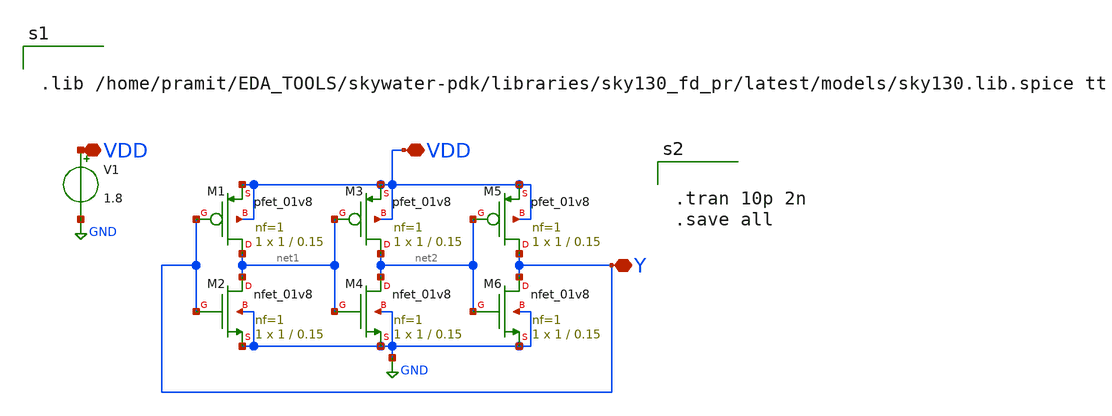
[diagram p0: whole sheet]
** sch_path: week4/schematic/ring_osc.sch
**.subckt ring_osc VDD Y VDD
*.iopin VDD
*.iopin Y
*.iopin VDD
XM1 net1 Y VDD VDD sky130_fd_pr__pfet_01v8 L=0.15 W=1 nf=1 ad='int((nf+1)/2) * W/nf * 0.29' as='int((nf+2)/2) * W/nf * 0.29'
+ pd='2*int((nf+1)/2) * (W/nf + 0.29)' ps='2*int((nf+2)/2) * (W/nf + 0.29)' nrd='0.29 / W' nrs='0.29 / W'
+ sa=0 sb=0 sd=0 mult=1 m=1
XM2 net1 Y GND GND sky130_fd_pr__nfet_01v8 L=0.15 W=1 nf=1 ad='int((nf+1)/2) * W/nf * 0.29' as='int((nf+2)/2) * W/nf * 0.29'
+ pd='2*int((nf+1)/2) * (W/nf + 0.29)' ps='2*int((nf+2)/2) * (W/nf + 0.29)' nrd='0.29 / W' nrs='0.29 / W'
+ sa=0 sb=0 sd=0 mult=1 m=1
XM3 net2 net1 VDD VDD sky130_fd_pr__pfet_01v8 L=0.15 W=1 nf=1 ad='int((nf+1)/2) * W/nf * 0.29' as='int((nf+2)/2) * W/nf * 0.29'
+ pd='2*int((nf+1)/2) * (W/nf + 0.29)' ps='2*int((nf+2)/2) * (W/nf + 0.29)' nrd='0.29 / W' nrs='0.29 / W'
+ sa=0 sb=0 sd=0 mult=1 m=1
XM4 net2 net1 GND GND sky130_fd_pr__nfet_01v8 L=0.15 W=1 nf=1 ad='int((nf+1)/2) * W/nf * 0.29' as='int((nf+2)/2) * W/nf * 0.29'
+ pd='2*int((nf+1)/2) * (W/nf + 0.29)' ps='2*int((nf+2)/2) * (W/nf + 0.29)' nrd='0.29 / W' nrs='0.29 / W'
+ sa=0 sb=0 sd=0 mult=1 m=1
XM5 Y net2 VDD VDD sky130_fd_pr__pfet_01v8 L=0.15 W=1 nf=1 ad='int((nf+1)/2) * W/nf * 0.29' as='int((nf+2)/2) * W/nf * 0.29'
+ pd='2*int((nf+1)/2) * (W/nf + 0.29)' ps='2*int((nf+2)/2) * (W/nf + 0.29)' nrd='0.29 / W' nrs='0.29 / W'
+ sa=0 sb=0 sd=0 mult=1 m=1
XM6 Y net2 GND GND sky130_fd_pr__nfet_01v8 L=0.15 W=1 nf=1 ad='int((nf+1)/2) * W/nf * 0.29' as='int((nf+2)/2) * W/nf * 0.29'
+ pd='2*int((nf+1)/2) * (W/nf + 0.29)' ps='2*int((nf+2)/2) * (W/nf + 0.29)' nrd='0.29 / W' nrs='0.29 / W'
+ sa=0 sb=0 sd=0 mult=1 m=1
V1 VDD GND 1.8
**** begin user architecture code


.lib /home/pramit/EDA_TOOLS/skywater-pdk/libraries/sky130_fd_pr/latest/models/sky130.lib.spice tt




.tran 10p 2n
.save all


**** end user architecture code
**.ends
.GLOBAL GND
.end
